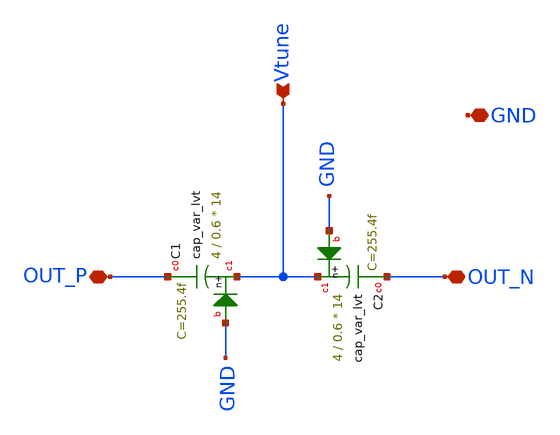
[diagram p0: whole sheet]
** sch_path: xschem/vco/parts/cap_var.sch
**.subckt cap_var OUT_P OUT_N GND Vtune
*.iopin OUT_P
*.iopin OUT_N
*.iopin GND
*.ipin Vtune
XC1 OUT_P Vtune GND sky130_fd_pr__cap_var_lvt W=4 L=0.6 VM=14 m=14
XC2 OUT_N Vtune GND sky130_fd_pr__cap_var_lvt W=4 L=0.6 VM=14 m=14
**.ends
.end
